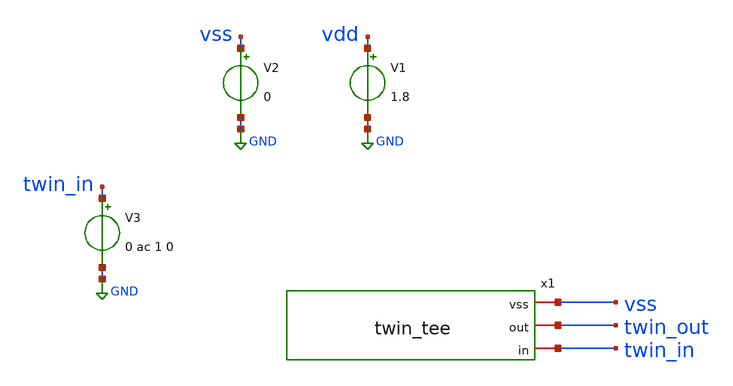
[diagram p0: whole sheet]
** sch_path: xschem/tb_twin_tee.sch
**.subckt tb_twin_tee
V1 vdd GND 1.8
V2 vss GND 0
V3 twin_in GND 0 ac 1 0
x1 vss twin_out twin_in twin_tee
**** begin user architecture code

** opencircuitdesign pdks install
.lib $::SKYWATER_MODELS/sky130.lib.spice tt
.include $::SKYWATER_STDCELLS/sky130_fd_sc_hd.spice





.param mc_mm_switch=0
.control
ac dec 100 1 100e7
*  tran 500p 2u uic
  write testbench.raw
  set appendwrite


.endc


**** end user architecture code
**.ends

* expanding   symbol:  twin_tee.sym # of pins=3
** sym_path: xschem/twin_tee.sym
** sch_path: xschem/twin_tee.sch
.subckt twin_tee vss out in
*.iopin vss
*.iopin in
*.iopin out
XR5 c1_c2 out vss sky130_fd_pr__res_high_po_0p35 L=50 mult=1 m=1
XC1 vss c1_c2 sky130_fd_pr__cap_mim_m3_1 W=15 L=15 MF=1 m=1
XC2 vss c1_c2 sky130_fd_pr__cap_mim_m3_1 W=15 L=15 MF=1 m=1
XR4 in c1_c2 vss sky130_fd_pr__res_high_po_0p35 L=50 mult=1 m=1
XC3 in c3_c4 sky130_fd_pr__cap_mim_m3_1 W=15 L=15 MF=1 m=1
XC4 c3_c4 out sky130_fd_pr__cap_mim_m3_1 W=15 L=15 MF=1 m=1
XR6 c3_c4 vss vss sky130_fd_pr__res_high_po_0p35 L=23 mult=1 m=1
.ends

.GLOBAL GND
.end
